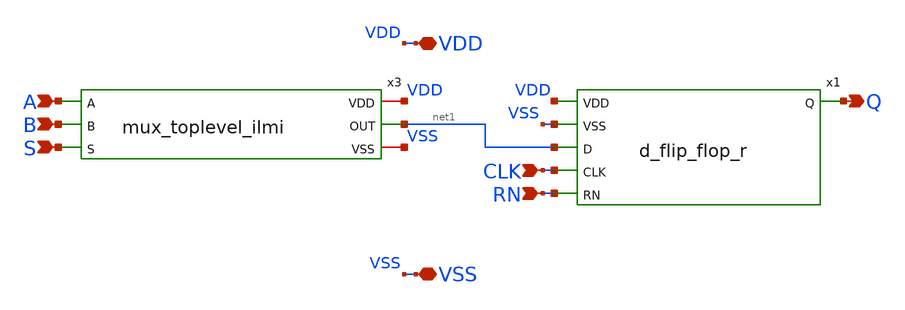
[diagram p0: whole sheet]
** sch_path: designs/libs/core_digital/sdffrq_tg_toplevel_ilmi/sdffrq_var_tg_toplevel.sch
**.subckt sdffrq_var_tg_toplevel A B S VDD VSS Q RN CLK
*.ipin A
*.ipin B
*.ipin S
*.iopin VDD
*.iopin VSS
*.opin Q
*.ipin RN
*.ipin CLK
x3 VDD A net1 B VSS S mux_toplevel_ilmi
x1 VDD VSS Q net1 CLK RN d_flip_flop_r
**.ends
.end
